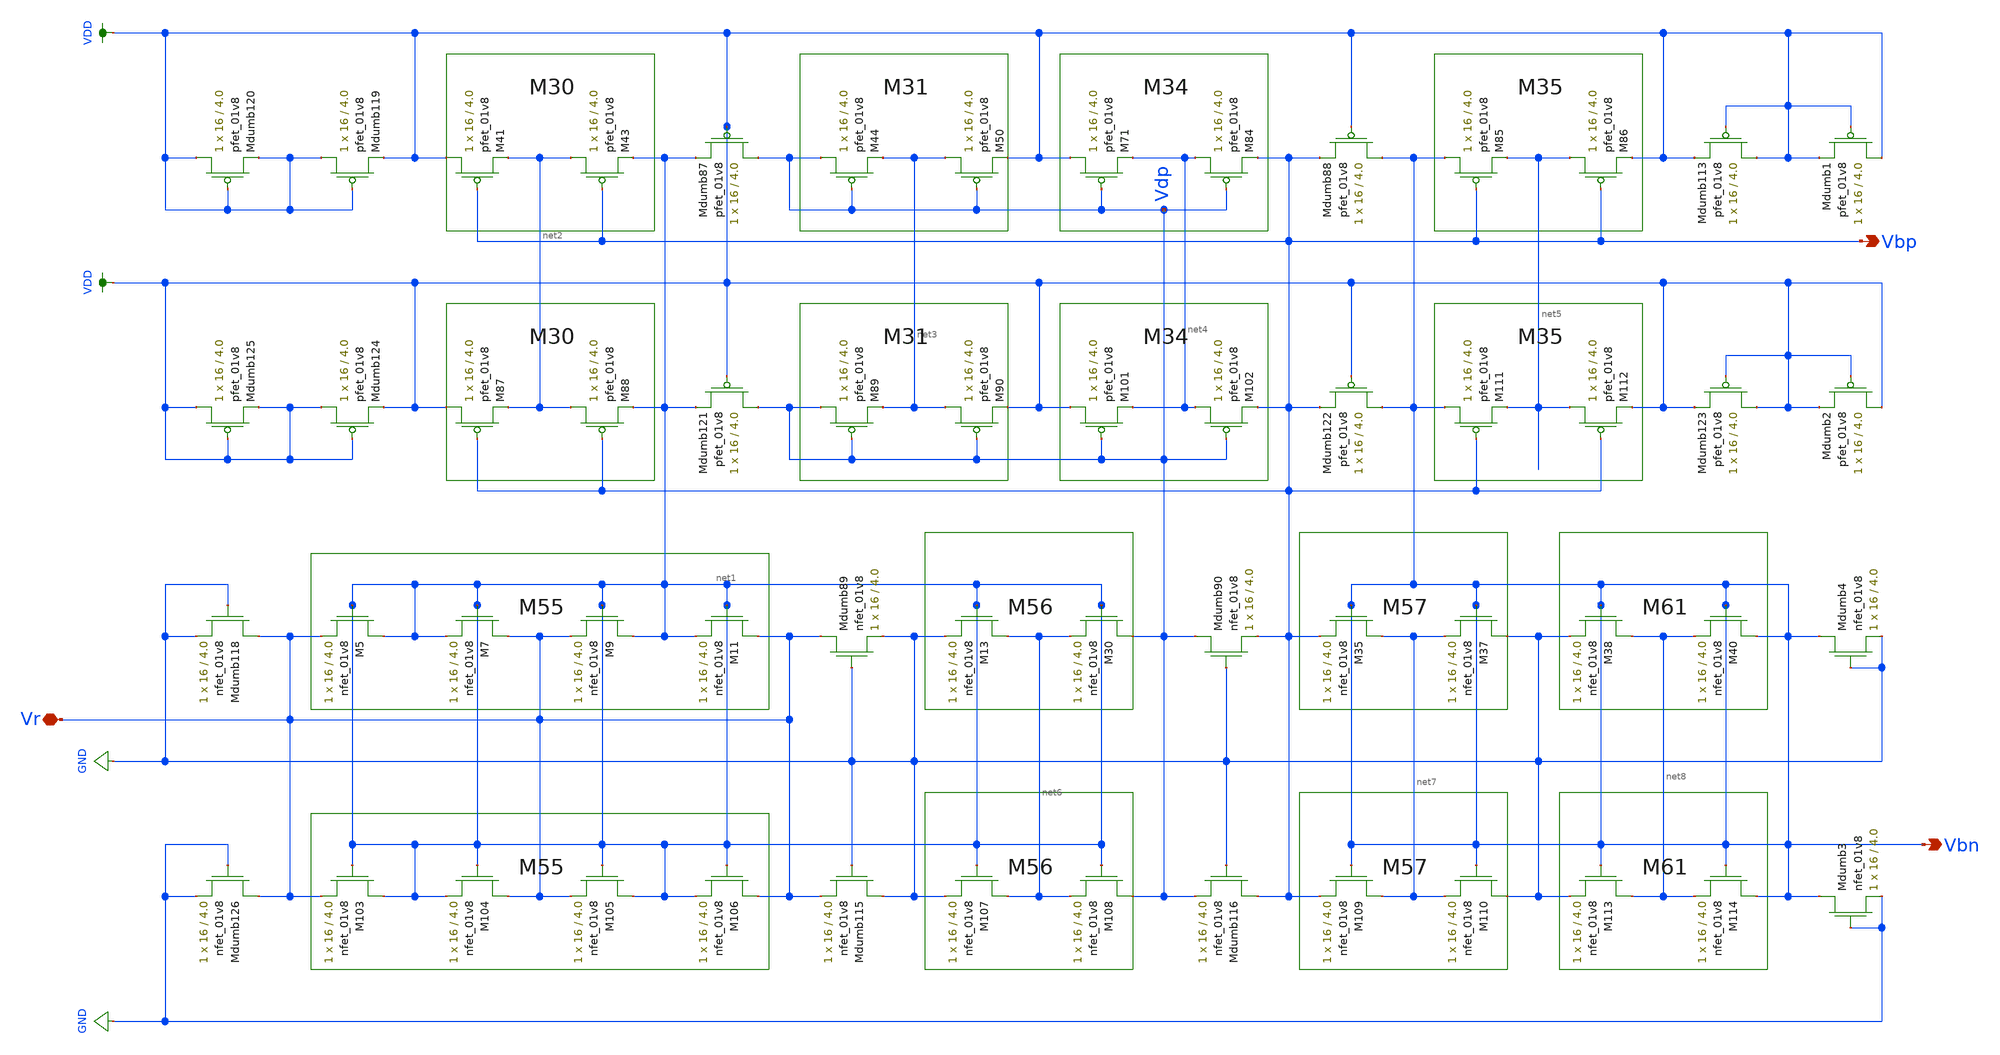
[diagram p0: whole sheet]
** sch_path: schematic/LDS/ibias.sch
**.subckt ibias Vr Vbp Vbn
*.iopin Vr
*.opin Vbp
*.opin Vbn
XM5 net1 net1 Vr GND sky130_fd_pr__nfet_01v8 L=4.0 W=16 nf=1 ad='int((nf+1)/2) * W/nf * 0.29' as='int((nf+2)/2) * W/nf * 0.29'
+ pd='2*int((nf+1)/2) * (W/nf + 0.29)' ps='2*int((nf+2)/2) * (W/nf + 0.29)' nrd='0.29 / W' nrs='0.29 / W'
+ sa=0 sb=0 sd=0 mult=1 m=1
XM7 Vr net1 net1 GND sky130_fd_pr__nfet_01v8 L=4.0 W=16 nf=1 ad='int((nf+1)/2) * W/nf * 0.29' as='int((nf+2)/2) * W/nf * 0.29'
+ pd='2*int((nf+1)/2) * (W/nf + 0.29)' ps='2*int((nf+2)/2) * (W/nf + 0.29)' nrd='0.29 / W' nrs='0.29 / W'
+ sa=0 sb=0 sd=0 mult=1 m=1
XM9 net1 net1 Vr GND sky130_fd_pr__nfet_01v8 L=4.0 W=16 nf=1 ad='int((nf+1)/2) * W/nf * 0.29' as='int((nf+2)/2) * W/nf * 0.29'
+ pd='2*int((nf+1)/2) * (W/nf + 0.29)' ps='2*int((nf+2)/2) * (W/nf + 0.29)' nrd='0.29 / W' nrs='0.29 / W'
+ sa=0 sb=0 sd=0 mult=1 m=1
XM11 Vr net1 net1 GND sky130_fd_pr__nfet_01v8 L=4.0 W=16 nf=1 ad='int((nf+1)/2) * W/nf * 0.29' as='int((nf+2)/2) * W/nf * 0.29'
+ pd='2*int((nf+1)/2) * (W/nf + 0.29)' ps='2*int((nf+2)/2) * (W/nf + 0.29)' nrd='0.29 / W' nrs='0.29 / W'
+ sa=0 sb=0 sd=0 mult=1 m=1
XM13 net6 net1 GND GND sky130_fd_pr__nfet_01v8 L=4.0 W=16 nf=1 ad='int((nf+1)/2) * W/nf * 0.29' as='int((nf+2)/2) * W/nf * 0.29'
+ pd='2*int((nf+1)/2) * (W/nf + 0.29)' ps='2*int((nf+2)/2) * (W/nf + 0.29)' nrd='0.29 / W' nrs='0.29 / W'
+ sa=0 sb=0 sd=0 mult=1 m=1
XM30 Vdp net1 net6 GND sky130_fd_pr__nfet_01v8 L=4.0 W=16 nf=1 ad='int((nf+1)/2) * W/nf * 0.29' as='int((nf+2)/2) * W/nf * 0.29'
+ pd='2*int((nf+1)/2) * (W/nf + 0.29)' ps='2*int((nf+2)/2) * (W/nf + 0.29)' nrd='0.29 / W' nrs='0.29 / W'
+ sa=0 sb=0 sd=0 mult=1 m=1
XM35 net7 Vbn Vbp GND sky130_fd_pr__nfet_01v8 L=4.0 W=16 nf=1 ad='int((nf+1)/2) * W/nf * 0.29' as='int((nf+2)/2) * W/nf * 0.29'
+ pd='2*int((nf+1)/2) * (W/nf + 0.29)' ps='2*int((nf+2)/2) * (W/nf + 0.29)' nrd='0.29 / W' nrs='0.29 / W'
+ sa=0 sb=0 sd=0 mult=1 m=1
XM37 GND Vbn net7 GND sky130_fd_pr__nfet_01v8 L=4.0 W=16 nf=1 ad='int((nf+1)/2) * W/nf * 0.29' as='int((nf+2)/2) * W/nf * 0.29'
+ pd='2*int((nf+1)/2) * (W/nf + 0.29)' ps='2*int((nf+2)/2) * (W/nf + 0.29)' nrd='0.29 / W' nrs='0.29 / W'
+ sa=0 sb=0 sd=0 mult=1 m=1
XM38 net8 Vbn GND GND sky130_fd_pr__nfet_01v8 L=4.0 W=16 nf=1 ad='int((nf+1)/2) * W/nf * 0.29' as='int((nf+2)/2) * W/nf * 0.29'
+ pd='2*int((nf+1)/2) * (W/nf + 0.29)' ps='2*int((nf+2)/2) * (W/nf + 0.29)' nrd='0.29 / W' nrs='0.29 / W'
+ sa=0 sb=0 sd=0 mult=1 m=1
XM40 Vbn Vbn net8 GND sky130_fd_pr__nfet_01v8 L=4.0 W=16 nf=1 ad='int((nf+1)/2) * W/nf * 0.29' as='int((nf+2)/2) * W/nf * 0.29'
+ pd='2*int((nf+1)/2) * (W/nf + 0.29)' ps='2*int((nf+2)/2) * (W/nf + 0.29)' nrd='0.29 / W' nrs='0.29 / W'
+ sa=0 sb=0 sd=0 mult=1 m=1
XM41 VDD Vbp net2 VDD sky130_fd_pr__pfet_01v8 L=4.0 W=16 nf=1 ad='int((nf+1)/2) * W/nf * 0.29' as='int((nf+2)/2) * W/nf * 0.29'
+ pd='2*int((nf+1)/2) * (W/nf + 0.29)' ps='2*int((nf+2)/2) * (W/nf + 0.29)' nrd='0.29 / W' nrs='0.29 / W'
+ sa=0 sb=0 sd=0 mult=1 m=1
XM43 net2 Vbp net1 VDD sky130_fd_pr__pfet_01v8 L=4.0 W=16 nf=1 ad='int((nf+1)/2) * W/nf * 0.29' as='int((nf+2)/2) * W/nf * 0.29'
+ pd='2*int((nf+1)/2) * (W/nf + 0.29)' ps='2*int((nf+2)/2) * (W/nf + 0.29)' nrd='0.29 / W' nrs='0.29 / W'
+ sa=0 sb=0 sd=0 mult=1 m=1
XM44 Vdp Vdp net3 VDD sky130_fd_pr__pfet_01v8 L=4.0 W=16 nf=1 ad='int((nf+1)/2) * W/nf * 0.29' as='int((nf+2)/2) * W/nf * 0.29'
+ pd='2*int((nf+1)/2) * (W/nf + 0.29)' ps='2*int((nf+2)/2) * (W/nf + 0.29)' nrd='0.29 / W' nrs='0.29 / W'
+ sa=0 sb=0 sd=0 mult=1 m=1
XM50 net3 Vdp VDD VDD sky130_fd_pr__pfet_01v8 L=4.0 W=16 nf=1 ad='int((nf+1)/2) * W/nf * 0.29' as='int((nf+2)/2) * W/nf * 0.29'
+ pd='2*int((nf+1)/2) * (W/nf + 0.29)' ps='2*int((nf+2)/2) * (W/nf + 0.29)' nrd='0.29 / W' nrs='0.29 / W'
+ sa=0 sb=0 sd=0 mult=1 m=1
XM71 VDD Vdp net4 VDD sky130_fd_pr__pfet_01v8 L=4.0 W=16 nf=1 ad='int((nf+1)/2) * W/nf * 0.29' as='int((nf+2)/2) * W/nf * 0.29'
+ pd='2*int((nf+1)/2) * (W/nf + 0.29)' ps='2*int((nf+2)/2) * (W/nf + 0.29)' nrd='0.29 / W' nrs='0.29 / W'
+ sa=0 sb=0 sd=0 mult=1 m=1
XM84 net4 Vdp Vbp VDD sky130_fd_pr__pfet_01v8 L=4.0 W=16 nf=1 ad='int((nf+1)/2) * W/nf * 0.29' as='int((nf+2)/2) * W/nf * 0.29'
+ pd='2*int((nf+1)/2) * (W/nf + 0.29)' ps='2*int((nf+2)/2) * (W/nf + 0.29)' nrd='0.29 / W' nrs='0.29 / W'
+ sa=0 sb=0 sd=0 mult=1 m=1
XM85 Vbn Vbp net5 VDD sky130_fd_pr__pfet_01v8 L=4.0 W=16 nf=1 ad='int((nf+1)/2) * W/nf * 0.29' as='int((nf+2)/2) * W/nf * 0.29'
+ pd='2*int((nf+1)/2) * (W/nf + 0.29)' ps='2*int((nf+2)/2) * (W/nf + 0.29)' nrd='0.29 / W' nrs='0.29 / W'
+ sa=0 sb=0 sd=0 mult=1 m=1
XM86 net5 Vbp VDD VDD sky130_fd_pr__pfet_01v8 L=4.0 W=16 nf=1 ad='int((nf+1)/2) * W/nf * 0.29' as='int((nf+2)/2) * W/nf * 0.29'
+ pd='2*int((nf+1)/2) * (W/nf + 0.29)' ps='2*int((nf+2)/2) * (W/nf + 0.29)' nrd='0.29 / W' nrs='0.29 / W'
+ sa=0 sb=0 sd=0 mult=1 m=1
XMdumb87 Vdp VDD net1 VDD sky130_fd_pr__pfet_01v8 L=4.0 W=16 nf=1 ad='int((nf+1)/2) * W/nf * 0.29' as='int((nf+2)/2) * W/nf * 0.29'
+ pd='2*int((nf+1)/2) * (W/nf + 0.29)' ps='2*int((nf+2)/2) * (W/nf + 0.29)' nrd='0.29 / W' nrs='0.29 / W'
+ sa=0 sb=0 sd=0 mult=1 m=1
XMdumb88 Vbn VDD Vbp VDD sky130_fd_pr__pfet_01v8 L=4.0 W=16 nf=1 ad='int((nf+1)/2) * W/nf * 0.29' as='int((nf+2)/2) * W/nf * 0.29'
+ pd='2*int((nf+1)/2) * (W/nf + 0.29)' ps='2*int((nf+2)/2) * (W/nf + 0.29)' nrd='0.29 / W' nrs='0.29 / W'
+ sa=0 sb=0 sd=0 mult=1 m=1
XMdumb89 Vr GND GND GND sky130_fd_pr__nfet_01v8 L=4.0 W=16 nf=1 ad='int((nf+1)/2) * W/nf * 0.29' as='int((nf+2)/2) * W/nf * 0.29'
+ pd='2*int((nf+1)/2) * (W/nf + 0.29)' ps='2*int((nf+2)/2) * (W/nf + 0.29)' nrd='0.29 / W' nrs='0.29 / W'
+ sa=0 sb=0 sd=0 mult=1 m=1
XMdumb90 Vdp GND Vbp GND sky130_fd_pr__nfet_01v8 L=4.0 W=16 nf=1 ad='int((nf+1)/2) * W/nf * 0.29' as='int((nf+2)/2) * W/nf * 0.29'
+ pd='2*int((nf+1)/2) * (W/nf + 0.29)' ps='2*int((nf+2)/2) * (W/nf + 0.29)' nrd='0.29 / W' nrs='0.29 / W'
+ sa=0 sb=0 sd=0 mult=1 m=1
XMdumb113 VDD VDD VDD VDD sky130_fd_pr__pfet_01v8 L=4.0 W=16 nf=1 ad='int((nf+1)/2) * W/nf * 0.29' as='int((nf+2)/2) * W/nf * 0.29'
+ pd='2*int((nf+1)/2) * (W/nf + 0.29)' ps='2*int((nf+2)/2) * (W/nf + 0.29)' nrd='0.29 / W' nrs='0.29 / W'
+ sa=0 sb=0 sd=0 mult=1 m=1
XMdumb118 Vr GND GND GND sky130_fd_pr__nfet_01v8 L=4.0 W=16 nf=1 ad='int((nf+1)/2) * W/nf * 0.29' as='int((nf+2)/2) * W/nf * 0.29'
+ pd='2*int((nf+1)/2) * (W/nf + 0.29)' ps='2*int((nf+2)/2) * (W/nf + 0.29)' nrd='0.29 / W' nrs='0.29 / W'
+ sa=0 sb=0 sd=0 mult=1 m=1
XMdumb119 VDD VDD VDD VDD sky130_fd_pr__pfet_01v8 L=4.0 W=16 nf=1 ad='int((nf+1)/2) * W/nf * 0.29' as='int((nf+2)/2) * W/nf * 0.29'
+ pd='2*int((nf+1)/2) * (W/nf + 0.29)' ps='2*int((nf+2)/2) * (W/nf + 0.29)' nrd='0.29 / W' nrs='0.29 / W'
+ sa=0 sb=0 sd=0 mult=1 m=1
XMdumb120 VDD VDD VDD VDD sky130_fd_pr__pfet_01v8 L=4.0 W=16 nf=1 ad='int((nf+1)/2) * W/nf * 0.29' as='int((nf+2)/2) * W/nf * 0.29'
+ pd='2*int((nf+1)/2) * (W/nf + 0.29)' ps='2*int((nf+2)/2) * (W/nf + 0.29)' nrd='0.29 / W' nrs='0.29 / W'
+ sa=0 sb=0 sd=0 mult=1 m=1
XM87 VDD Vbp net2 VDD sky130_fd_pr__pfet_01v8 L=4.0 W=16 nf=1 ad='int((nf+1)/2) * W/nf * 0.29' as='int((nf+2)/2) * W/nf * 0.29'
+ pd='2*int((nf+1)/2) * (W/nf + 0.29)' ps='2*int((nf+2)/2) * (W/nf + 0.29)' nrd='0.29 / W' nrs='0.29 / W'
+ sa=0 sb=0 sd=0 mult=1 m=1
XM88 net2 Vbp net1 VDD sky130_fd_pr__pfet_01v8 L=4.0 W=16 nf=1 ad='int((nf+1)/2) * W/nf * 0.29' as='int((nf+2)/2) * W/nf * 0.29'
+ pd='2*int((nf+1)/2) * (W/nf + 0.29)' ps='2*int((nf+2)/2) * (W/nf + 0.29)' nrd='0.29 / W' nrs='0.29 / W'
+ sa=0 sb=0 sd=0 mult=1 m=1
XM89 Vdp Vdp net3 VDD sky130_fd_pr__pfet_01v8 L=4.0 W=16 nf=1 ad='int((nf+1)/2) * W/nf * 0.29' as='int((nf+2)/2) * W/nf * 0.29'
+ pd='2*int((nf+1)/2) * (W/nf + 0.29)' ps='2*int((nf+2)/2) * (W/nf + 0.29)' nrd='0.29 / W' nrs='0.29 / W'
+ sa=0 sb=0 sd=0 mult=1 m=1
XM90 net3 Vdp VDD VDD sky130_fd_pr__pfet_01v8 L=4.0 W=16 nf=1 ad='int((nf+1)/2) * W/nf * 0.29' as='int((nf+2)/2) * W/nf * 0.29'
+ pd='2*int((nf+1)/2) * (W/nf + 0.29)' ps='2*int((nf+2)/2) * (W/nf + 0.29)' nrd='0.29 / W' nrs='0.29 / W'
+ sa=0 sb=0 sd=0 mult=1 m=1
XM101 VDD Vdp net4 VDD sky130_fd_pr__pfet_01v8 L=4.0 W=16 nf=1 ad='int((nf+1)/2) * W/nf * 0.29' as='int((nf+2)/2) * W/nf * 0.29'
+ pd='2*int((nf+1)/2) * (W/nf + 0.29)' ps='2*int((nf+2)/2) * (W/nf + 0.29)' nrd='0.29 / W' nrs='0.29 / W'
+ sa=0 sb=0 sd=0 mult=1 m=1
XM102 net4 Vdp Vbp VDD sky130_fd_pr__pfet_01v8 L=4.0 W=16 nf=1 ad='int((nf+1)/2) * W/nf * 0.29' as='int((nf+2)/2) * W/nf * 0.29'
+ pd='2*int((nf+1)/2) * (W/nf + 0.29)' ps='2*int((nf+2)/2) * (W/nf + 0.29)' nrd='0.29 / W' nrs='0.29 / W'
+ sa=0 sb=0 sd=0 mult=1 m=1
XM111 Vbn Vbp net5 VDD sky130_fd_pr__pfet_01v8 L=4.0 W=16 nf=1 ad='int((nf+1)/2) * W/nf * 0.29' as='int((nf+2)/2) * W/nf * 0.29'
+ pd='2*int((nf+1)/2) * (W/nf + 0.29)' ps='2*int((nf+2)/2) * (W/nf + 0.29)' nrd='0.29 / W' nrs='0.29 / W'
+ sa=0 sb=0 sd=0 mult=1 m=1
XM112 net5 Vbp VDD VDD sky130_fd_pr__pfet_01v8 L=4.0 W=16 nf=1 ad='int((nf+1)/2) * W/nf * 0.29' as='int((nf+2)/2) * W/nf * 0.29'
+ pd='2*int((nf+1)/2) * (W/nf + 0.29)' ps='2*int((nf+2)/2) * (W/nf + 0.29)' nrd='0.29 / W' nrs='0.29 / W'
+ sa=0 sb=0 sd=0 mult=1 m=1
XMdumb121 Vdp VDD net1 VDD sky130_fd_pr__pfet_01v8 L=4.0 W=16 nf=1 ad='int((nf+1)/2) * W/nf * 0.29' as='int((nf+2)/2) * W/nf * 0.29'
+ pd='2*int((nf+1)/2) * (W/nf + 0.29)' ps='2*int((nf+2)/2) * (W/nf + 0.29)' nrd='0.29 / W' nrs='0.29 / W'
+ sa=0 sb=0 sd=0 mult=1 m=1
XMdumb122 Vbn VDD Vbp VDD sky130_fd_pr__pfet_01v8 L=4.0 W=16 nf=1 ad='int((nf+1)/2) * W/nf * 0.29' as='int((nf+2)/2) * W/nf * 0.29'
+ pd='2*int((nf+1)/2) * (W/nf + 0.29)' ps='2*int((nf+2)/2) * (W/nf + 0.29)' nrd='0.29 / W' nrs='0.29 / W'
+ sa=0 sb=0 sd=0 mult=1 m=1
XMdumb123 VDD VDD VDD VDD sky130_fd_pr__pfet_01v8 L=4.0 W=16 nf=1 ad='int((nf+1)/2) * W/nf * 0.29' as='int((nf+2)/2) * W/nf * 0.29'
+ pd='2*int((nf+1)/2) * (W/nf + 0.29)' ps='2*int((nf+2)/2) * (W/nf + 0.29)' nrd='0.29 / W' nrs='0.29 / W'
+ sa=0 sb=0 sd=0 mult=1 m=1
XMdumb124 VDD VDD VDD VDD sky130_fd_pr__pfet_01v8 L=4.0 W=16 nf=1 ad='int((nf+1)/2) * W/nf * 0.29' as='int((nf+2)/2) * W/nf * 0.29'
+ pd='2*int((nf+1)/2) * (W/nf + 0.29)' ps='2*int((nf+2)/2) * (W/nf + 0.29)' nrd='0.29 / W' nrs='0.29 / W'
+ sa=0 sb=0 sd=0 mult=1 m=1
XMdumb125 VDD VDD VDD VDD sky130_fd_pr__pfet_01v8 L=4.0 W=16 nf=1 ad='int((nf+1)/2) * W/nf * 0.29' as='int((nf+2)/2) * W/nf * 0.29'
+ pd='2*int((nf+1)/2) * (W/nf + 0.29)' ps='2*int((nf+2)/2) * (W/nf + 0.29)' nrd='0.29 / W' nrs='0.29 / W'
+ sa=0 sb=0 sd=0 mult=1 m=1
XM103 net1 net1 Vr GND sky130_fd_pr__nfet_01v8 L=4.0 W=16 nf=1 ad='int((nf+1)/2) * W/nf * 0.29' as='int((nf+2)/2) * W/nf * 0.29'
+ pd='2*int((nf+1)/2) * (W/nf + 0.29)' ps='2*int((nf+2)/2) * (W/nf + 0.29)' nrd='0.29 / W' nrs='0.29 / W'
+ sa=0 sb=0 sd=0 mult=1 m=1
XM104 Vr net1 net1 GND sky130_fd_pr__nfet_01v8 L=4.0 W=16 nf=1 ad='int((nf+1)/2) * W/nf * 0.29' as='int((nf+2)/2) * W/nf * 0.29'
+ pd='2*int((nf+1)/2) * (W/nf + 0.29)' ps='2*int((nf+2)/2) * (W/nf + 0.29)' nrd='0.29 / W' nrs='0.29 / W'
+ sa=0 sb=0 sd=0 mult=1 m=1
XM105 net1 net1 Vr GND sky130_fd_pr__nfet_01v8 L=4.0 W=16 nf=1 ad='int((nf+1)/2) * W/nf * 0.29' as='int((nf+2)/2) * W/nf * 0.29'
+ pd='2*int((nf+1)/2) * (W/nf + 0.29)' ps='2*int((nf+2)/2) * (W/nf + 0.29)' nrd='0.29 / W' nrs='0.29 / W'
+ sa=0 sb=0 sd=0 mult=1 m=1
XM106 Vr net1 net1 GND sky130_fd_pr__nfet_01v8 L=4.0 W=16 nf=1 ad='int((nf+1)/2) * W/nf * 0.29' as='int((nf+2)/2) * W/nf * 0.29'
+ pd='2*int((nf+1)/2) * (W/nf + 0.29)' ps='2*int((nf+2)/2) * (W/nf + 0.29)' nrd='0.29 / W' nrs='0.29 / W'
+ sa=0 sb=0 sd=0 mult=1 m=1
XM107 net6 net1 GND GND sky130_fd_pr__nfet_01v8 L=4.0 W=16 nf=1 ad='int((nf+1)/2) * W/nf * 0.29' as='int((nf+2)/2) * W/nf * 0.29'
+ pd='2*int((nf+1)/2) * (W/nf + 0.29)' ps='2*int((nf+2)/2) * (W/nf + 0.29)' nrd='0.29 / W' nrs='0.29 / W'
+ sa=0 sb=0 sd=0 mult=1 m=1
XM108 Vdp net1 net6 GND sky130_fd_pr__nfet_01v8 L=4.0 W=16 nf=1 ad='int((nf+1)/2) * W/nf * 0.29' as='int((nf+2)/2) * W/nf * 0.29'
+ pd='2*int((nf+1)/2) * (W/nf + 0.29)' ps='2*int((nf+2)/2) * (W/nf + 0.29)' nrd='0.29 / W' nrs='0.29 / W'
+ sa=0 sb=0 sd=0 mult=1 m=1
XM109 net7 Vbn Vbp GND sky130_fd_pr__nfet_01v8 L=4.0 W=16 nf=1 ad='int((nf+1)/2) * W/nf * 0.29' as='int((nf+2)/2) * W/nf * 0.29'
+ pd='2*int((nf+1)/2) * (W/nf + 0.29)' ps='2*int((nf+2)/2) * (W/nf + 0.29)' nrd='0.29 / W' nrs='0.29 / W'
+ sa=0 sb=0 sd=0 mult=1 m=1
XM110 GND Vbn net7 GND sky130_fd_pr__nfet_01v8 L=4.0 W=16 nf=1 ad='int((nf+1)/2) * W/nf * 0.29' as='int((nf+2)/2) * W/nf * 0.29'
+ pd='2*int((nf+1)/2) * (W/nf + 0.29)' ps='2*int((nf+2)/2) * (W/nf + 0.29)' nrd='0.29 / W' nrs='0.29 / W'
+ sa=0 sb=0 sd=0 mult=1 m=1
XM113 net8 Vbn GND GND sky130_fd_pr__nfet_01v8 L=4.0 W=16 nf=1 ad='int((nf+1)/2) * W/nf * 0.29' as='int((nf+2)/2) * W/nf * 0.29'
+ pd='2*int((nf+1)/2) * (W/nf + 0.29)' ps='2*int((nf+2)/2) * (W/nf + 0.29)' nrd='0.29 / W' nrs='0.29 / W'
+ sa=0 sb=0 sd=0 mult=1 m=1
XM114 Vbn Vbn net8 GND sky130_fd_pr__nfet_01v8 L=4.0 W=16 nf=1 ad='int((nf+1)/2) * W/nf * 0.29' as='int((nf+2)/2) * W/nf * 0.29'
+ pd='2*int((nf+1)/2) * (W/nf + 0.29)' ps='2*int((nf+2)/2) * (W/nf + 0.29)' nrd='0.29 / W' nrs='0.29 / W'
+ sa=0 sb=0 sd=0 mult=1 m=1
XMdumb115 GND GND Vr GND sky130_fd_pr__nfet_01v8 L=4.0 W=16 nf=1 ad='int((nf+1)/2) * W/nf * 0.29' as='int((nf+2)/2) * W/nf * 0.29'
+ pd='2*int((nf+1)/2) * (W/nf + 0.29)' ps='2*int((nf+2)/2) * (W/nf + 0.29)' nrd='0.29 / W' nrs='0.29 / W'
+ sa=0 sb=0 sd=0 mult=1 m=1
XMdumb116 Vbp GND Vdp GND sky130_fd_pr__nfet_01v8 L=4.0 W=16 nf=1 ad='int((nf+1)/2) * W/nf * 0.29' as='int((nf+2)/2) * W/nf * 0.29'
+ pd='2*int((nf+1)/2) * (W/nf + 0.29)' ps='2*int((nf+2)/2) * (W/nf + 0.29)' nrd='0.29 / W' nrs='0.29 / W'
+ sa=0 sb=0 sd=0 mult=1 m=1
XMdumb126 Vr GND GND GND sky130_fd_pr__nfet_01v8 L=4.0 W=16 nf=1 ad='int((nf+1)/2) * W/nf * 0.29' as='int((nf+2)/2) * W/nf * 0.29'
+ pd='2*int((nf+1)/2) * (W/nf + 0.29)' ps='2*int((nf+2)/2) * (W/nf + 0.29)' nrd='0.29 / W' nrs='0.29 / W'
+ sa=0 sb=0 sd=0 mult=1 m=1
XMdumb1 VDD VDD VDD VDD sky130_fd_pr__pfet_01v8 L=4.0 W=16 nf=1 ad='int((nf+1)/2) * W/nf * 0.29' as='int((nf+2)/2) * W/nf * 0.29'
+ pd='2*int((nf+1)/2) * (W/nf + 0.29)' ps='2*int((nf+2)/2) * (W/nf + 0.29)' nrd='0.29 / W' nrs='0.29 / W'
+ sa=0 sb=0 sd=0 mult=1 m=1
XMdumb2 VDD VDD VDD VDD sky130_fd_pr__pfet_01v8 L=4.0 W=16 nf=1 ad='int((nf+1)/2) * W/nf * 0.29' as='int((nf+2)/2) * W/nf * 0.29'
+ pd='2*int((nf+1)/2) * (W/nf + 0.29)' ps='2*int((nf+2)/2) * (W/nf + 0.29)' nrd='0.29 / W' nrs='0.29 / W'
+ sa=0 sb=0 sd=0 mult=1 m=1
XMdumb3 Vbn GND GND GND sky130_fd_pr__nfet_01v8 L=4.0 W=16 nf=1 ad='int((nf+1)/2) * W/nf * 0.29' as='int((nf+2)/2) * W/nf * 0.29'
+ pd='2*int((nf+1)/2) * (W/nf + 0.29)' ps='2*int((nf+2)/2) * (W/nf + 0.29)' nrd='0.29 / W' nrs='0.29 / W'
+ sa=0 sb=0 sd=0 mult=1 m=1
XMdumb4 Vbn GND GND GND sky130_fd_pr__nfet_01v8 L=4.0 W=16 nf=1 ad='int((nf+1)/2) * W/nf * 0.29' as='int((nf+2)/2) * W/nf * 0.29'
+ pd='2*int((nf+1)/2) * (W/nf + 0.29)' ps='2*int((nf+2)/2) * (W/nf + 0.29)' nrd='0.29 / W' nrs='0.29 / W'
+ sa=0 sb=0 sd=0 mult=1 m=1
**.ends
.GLOBAL GND
.GLOBAL VDD
.end
